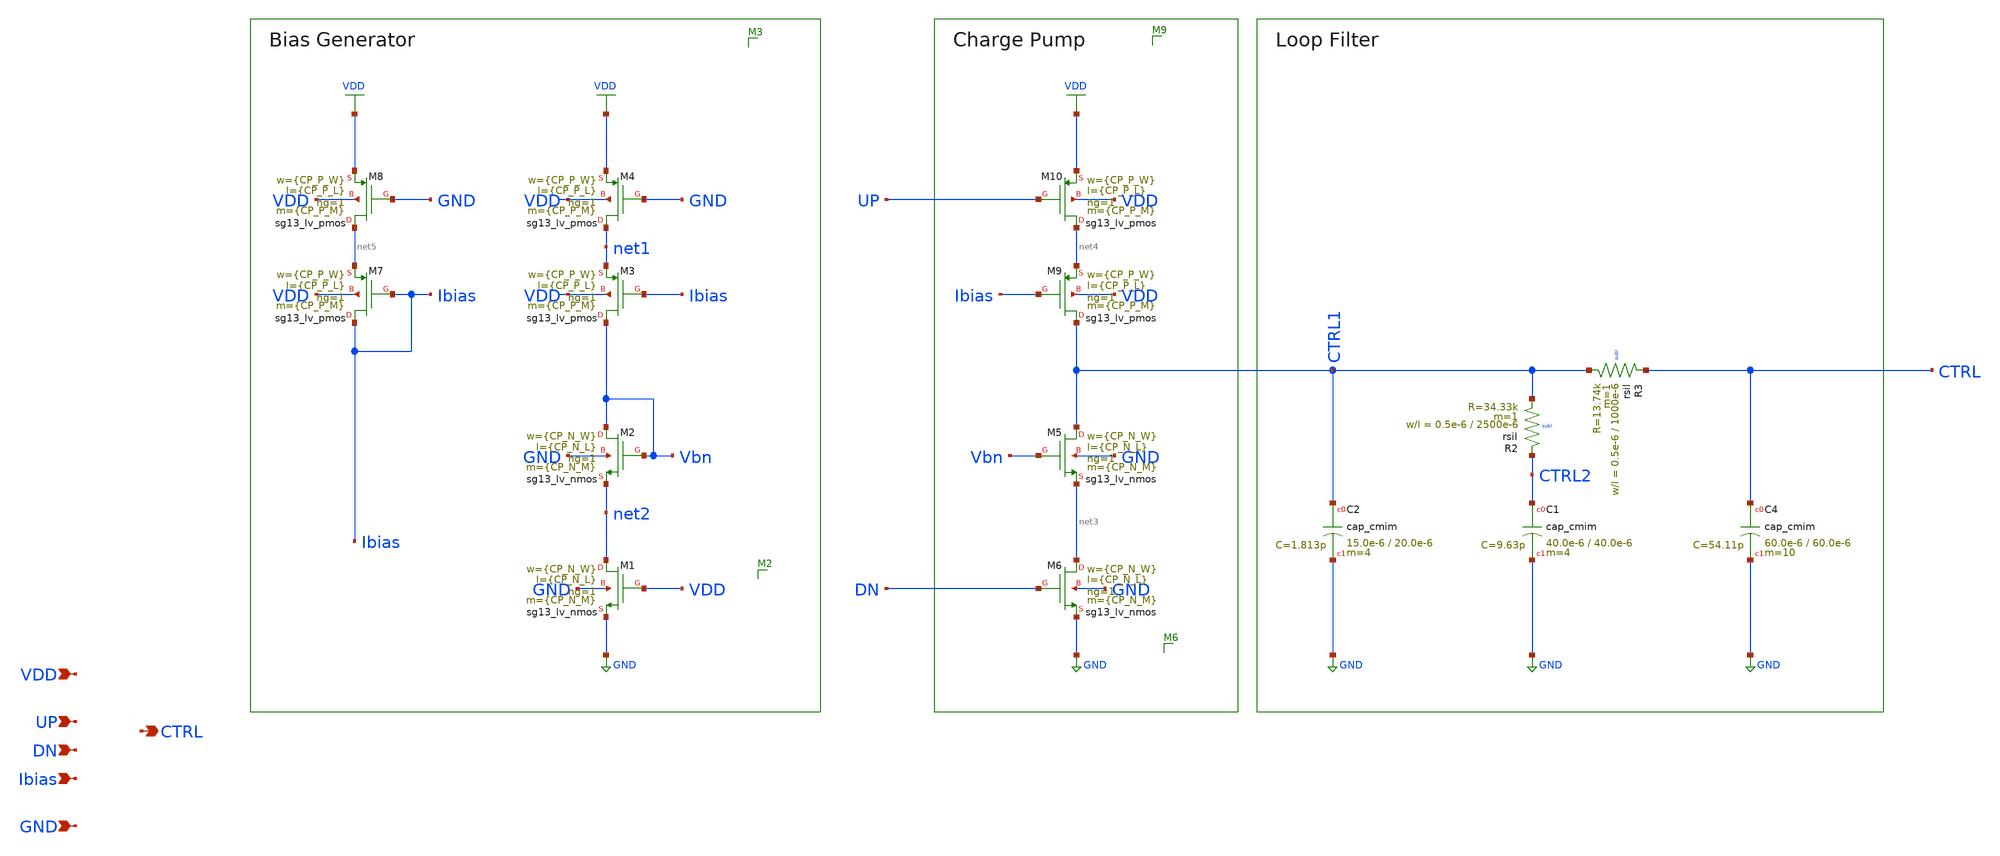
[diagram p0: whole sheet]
** sch_path: schematic/blocks/charge-pump/CP.sch
**.subckt CP CTRL UP VDD Ibias DN GND
*.opin CTRL
*.ipin UP
*.ipin VDD
*.ipin Ibias
*.ipin DN
*.ipin GND
XM2 Vbn Vbn net2 GND sg13_lv_nmos w={CP_N_W} l={CP_N_L} ng=1 m={CP_N_M} mm_ok=1
XM1 net2 VDD GND GND sg13_lv_nmos w={CP_N_W} l={CP_N_L} ng=1 m={CP_N_M} mm_ok=1
XM3 Vbn Ibias net1 VDD sg13_lv_pmos w={CP_P_W} l={CP_P_L} ng=1 m={CP_P_M} mm_ok=1
XM4 net1 GND VDD VDD sg13_lv_pmos w={CP_P_W} l={CP_P_L} ng=1 m={CP_P_M} mm_ok=1
XM7 Ibias Ibias net5 VDD sg13_lv_pmos w={CP_P_W} l={CP_P_L} ng=1 m={CP_P_M} mm_ok=1
XM8 net5 GND VDD VDD sg13_lv_pmos w={CP_P_W} l={CP_P_L} ng=1 m={CP_P_M} mm_ok=1
XM5 CTRL1 Vbn net3 GND sg13_lv_nmos w={CP_N_W} l={CP_N_L} ng=1 m={CP_N_M} mm_ok=1
XM6 net3 DN GND GND sg13_lv_nmos w={CP_N_W} l={CP_N_L} ng=1 m={CP_N_M} mm_ok=1
XM9 CTRL1 Ibias net4 VDD sg13_lv_pmos w={CP_P_W} l={CP_P_L} ng=1 m={CP_P_M} mm_ok=1
XM10 net4 UP VDD VDD sg13_lv_pmos w={CP_P_W} l={CP_P_L} ng=1 m={CP_P_M} mm_ok=1
XR3 CTRL CTRL1 sub! rsil w=0.5e-6 l=1000e-6 m=1 mm_ok=1
XR2 CTRL2 CTRL1 sub! rsil w=0.5e-6 l=2500e-6 m=1 mm_ok=1
XC4 CTRL GND cap_cmim w=60.0e-6 l=60.0e-6 m=10 mm_ok=1
XC1 CTRL2 GND cap_cmim w=40.0e-6 l=40.0e-6 m=4 mm_ok=1
XC2 CTRL1 GND cap_cmim w=15.0e-6 l=20.0e-6 m=4 mm_ok=1
**.ends
.GLOBAL GND
.GLOBAL VDD
.end
